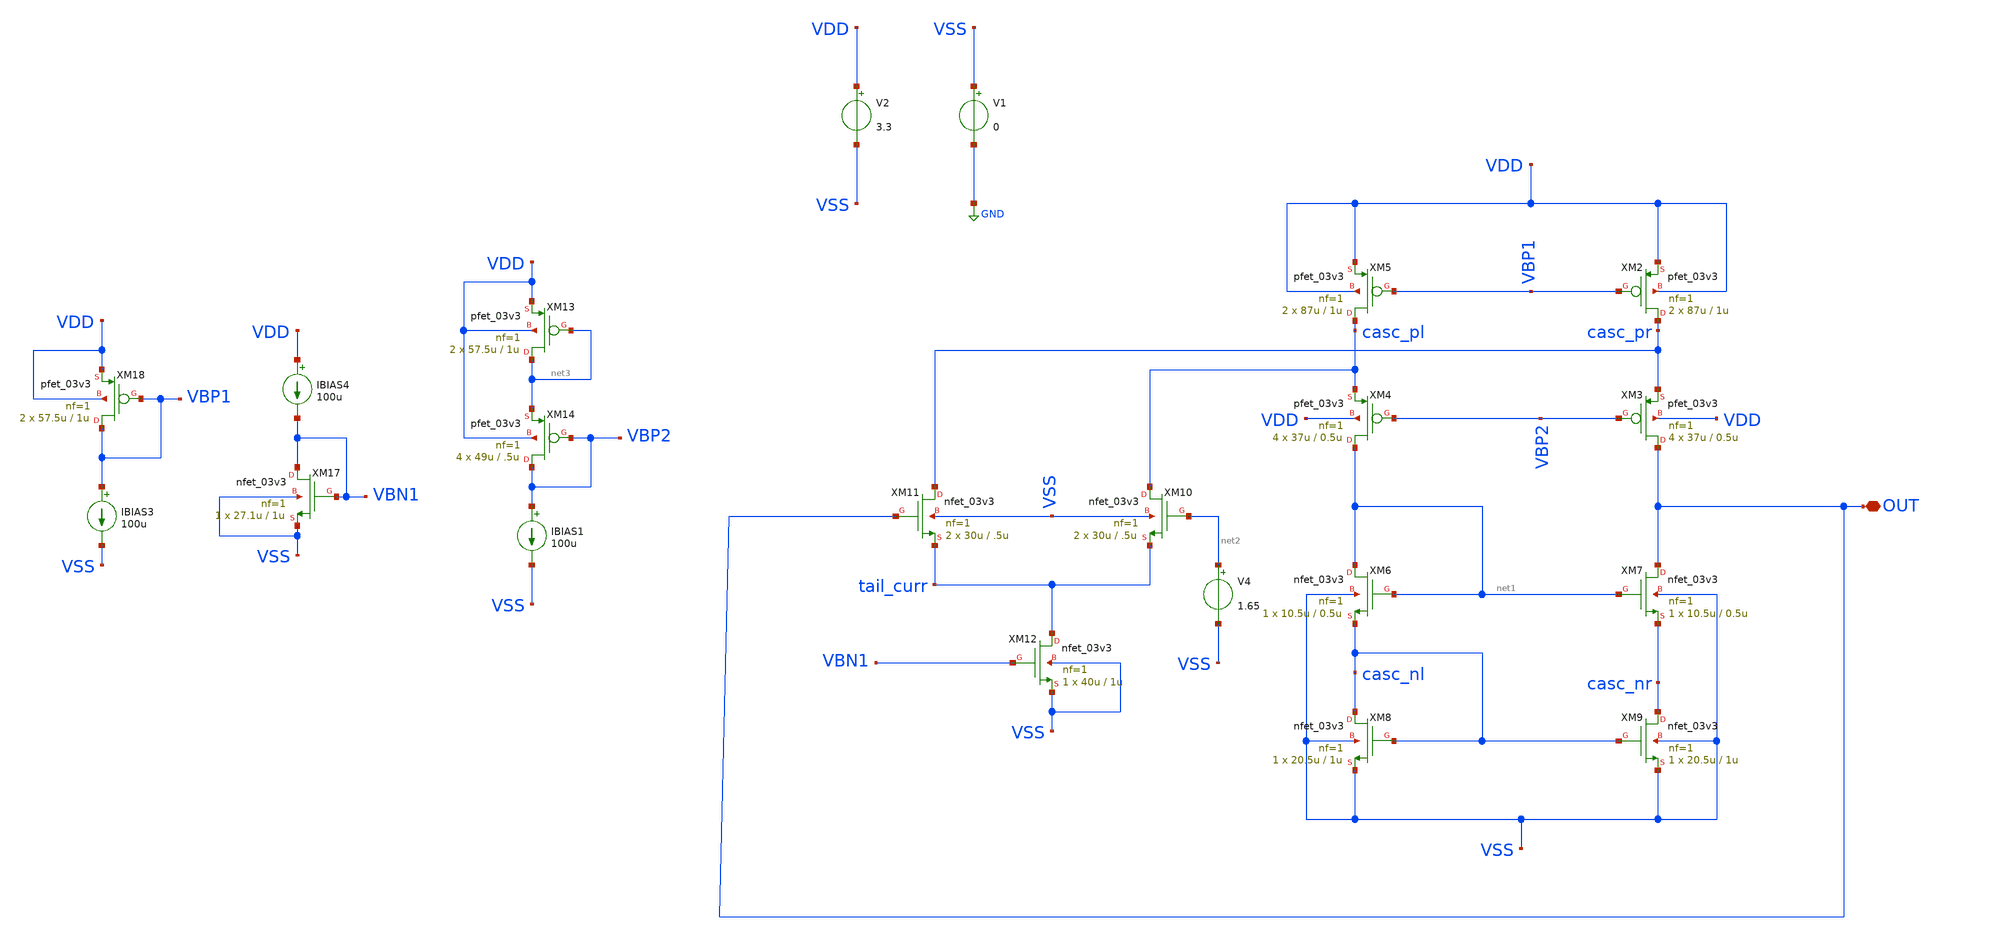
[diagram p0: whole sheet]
** sch_path: designs/untitled.sch
**.subckt untitled OUT
*.iopin OUT
XM2 casc_pr VBP1 VDD VDD pfet_03v3 L=1u W=87u nf=1 ad='int((nf+1)/2) * W/nf * 0.18u' as='int((nf+2)/2) * W/nf * 0.18u'
+ pd='2*int((nf+1)/2) * (W/nf + 0.18u)' ps='2*int((nf+2)/2) * (W/nf + 0.18u)' nrd='0.18u / W' nrs='0.18u / W'
+ sa=0 sb=0 sd=0 m=2
XM3 OUT VBP2 casc_pr VDD pfet_03v3 L=0.5u W=37u nf=1 ad='int((nf+1)/2) * W/nf * 0.18u' as='int((nf+2)/2) * W/nf * 0.18u'
+ pd='2*int((nf+1)/2) * (W/nf + 0.18u)' ps='2*int((nf+2)/2) * (W/nf + 0.18u)' nrd='0.18u / W' nrs='0.18u / W'
+ sa=0 sb=0 sd=0 m=4
XM4 net1 VBP2 casc_pl VDD pfet_03v3 L=0.5u W=37u nf=1 ad='int((nf+1)/2) * W/nf * 0.18u' as='int((nf+2)/2) * W/nf * 0.18u'
+ pd='2*int((nf+1)/2) * (W/nf + 0.18u)' ps='2*int((nf+2)/2) * (W/nf + 0.18u)' nrd='0.18u / W' nrs='0.18u / W'
+ sa=0 sb=0 sd=0 m=4
XM5 casc_pl VBP1 VDD VDD pfet_03v3 L=1u W=87u nf=1 ad='int((nf+1)/2) * W/nf * 0.18u' as='int((nf+2)/2) * W/nf * 0.18u'
+ pd='2*int((nf+1)/2) * (W/nf + 0.18u)' ps='2*int((nf+2)/2) * (W/nf + 0.18u)' nrd='0.18u / W' nrs='0.18u / W'
+ sa=0 sb=0 sd=0 m=2
XM6 net1 net1 casc_nl VSS nfet_03v3 L=0.5u W=10.5u nf=1 ad='int((nf+1)/2) * W/nf * 0.18u' as='int((nf+2)/2) * W/nf * 0.18u'
+ pd='2*int((nf+1)/2) * (W/nf + 0.18u)' ps='2*int((nf+2)/2) * (W/nf + 0.18u)' nrd='0.18u / W' nrs='0.18u / W'
+ sa=0 sb=0 sd=0 m=1
XM7 OUT net1 casc_nr VSS nfet_03v3 L=0.5u W=10.5u nf=1 ad='int((nf+1)/2) * W/nf * 0.18u' as='int((nf+2)/2) * W/nf * 0.18u'
+ pd='2*int((nf+1)/2) * (W/nf + 0.18u)' ps='2*int((nf+2)/2) * (W/nf + 0.18u)' nrd='0.18u / W' nrs='0.18u / W'
+ sa=0 sb=0 sd=0 m=1
XM8 casc_nl casc_nl VSS VSS nfet_03v3 L=1u W=20.5u nf=1 ad='int((nf+1)/2) * W/nf * 0.18u' as='int((nf+2)/2) * W/nf * 0.18u'
+ pd='2*int((nf+1)/2) * (W/nf + 0.18u)' ps='2*int((nf+2)/2) * (W/nf + 0.18u)' nrd='0.18u / W' nrs='0.18u / W'
+ sa=0 sb=0 sd=0 m=1
XM9 casc_nr casc_nl VSS VSS nfet_03v3 L=1u W=20.5u nf=1 ad='int((nf+1)/2) * W/nf * 0.18u' as='int((nf+2)/2) * W/nf * 0.18u'
+ pd='2*int((nf+1)/2) * (W/nf + 0.18u)' ps='2*int((nf+2)/2) * (W/nf + 0.18u)' nrd='0.18u / W' nrs='0.18u / W'
+ sa=0 sb=0 sd=0 m=1
XM10 casc_pl net2 tail_curr VSS nfet_03v3 L=.5u W=30u nf=1 ad='int((nf+1)/2) * W/nf * 0.18u' as='int((nf+2)/2) * W/nf * 0.18u'
+ pd='2*int((nf+1)/2) * (W/nf + 0.18u)' ps='2*int((nf+2)/2) * (W/nf + 0.18u)' nrd='0.18u / W' nrs='0.18u / W'
+ sa=0 sb=0 sd=0 m=2
XM12 tail_curr VBN1 VSS VSS nfet_03v3 L=1u W=40u nf=1 ad='int((nf+1)/2) * W/nf * 0.18u' as='int((nf+2)/2) * W/nf * 0.18u'
+ pd='2*int((nf+1)/2) * (W/nf + 0.18u)' ps='2*int((nf+2)/2) * (W/nf + 0.18u)' nrd='0.18u / W' nrs='0.18u / W'
+ sa=0 sb=0 sd=0 m=1
XM11 casc_pr OUT tail_curr VSS nfet_03v3 L=.5u W=30u nf=1 ad='int((nf+1)/2) * W/nf * 0.18u' as='int((nf+2)/2) * W/nf * 0.18u'
+ pd='2*int((nf+1)/2) * (W/nf + 0.18u)' ps='2*int((nf+2)/2) * (W/nf + 0.18u)' nrd='0.18u / W' nrs='0.18u / W'
+ sa=0 sb=0 sd=0 m=2
V2 VDD VSS 3.3
V1 VSS GND 0
V4 net2 VSS 1.65
XM13 net3 net3 VDD VDD pfet_03v3 L=1u W=57.5u nf=1 ad='int((nf+1)/2) * W/nf * 0.18u' as='int((nf+2)/2) * W/nf * 0.18u'
+ pd='2*int((nf+1)/2) * (W/nf + 0.18u)' ps='2*int((nf+2)/2) * (W/nf + 0.18u)' nrd='0.18u / W' nrs='0.18u / W'
+ sa=0 sb=0 sd=0 m=2
IBIAS1 VBP2 VSS 100u
XM14 VBP2 VBP2 net3 VDD pfet_03v3 L=.5u W=49u nf=1 ad='int((nf+1)/2) * W/nf * 0.18u' as='int((nf+2)/2) * W/nf * 0.18u'
+ pd='2*int((nf+1)/2) * (W/nf + 0.18u)' ps='2*int((nf+2)/2) * (W/nf + 0.18u)' nrd='0.18u / W' nrs='0.18u / W'
+ sa=0 sb=0 sd=0 m=4
XM17 VBN1 VBN1 VSS VSS nfet_03v3 L=1u W=27.1u nf=1 ad='int((nf+1)/2) * W/nf * 0.18u' as='int((nf+2)/2) * W/nf * 0.18u'
+ pd='2*int((nf+1)/2) * (W/nf + 0.18u)' ps='2*int((nf+2)/2) * (W/nf + 0.18u)' nrd='0.18u / W' nrs='0.18u / W'
+ sa=0 sb=0 sd=0 m=1
XM18 VBP1 VBP1 VDD VDD pfet_03v3 L=1u W=57.5u nf=1 ad='int((nf+1)/2) * W/nf * 0.18u' as='int((nf+2)/2) * W/nf * 0.18u'
+ pd='2*int((nf+1)/2) * (W/nf + 0.18u)' ps='2*int((nf+2)/2) * (W/nf + 0.18u)' nrd='0.18u / W' nrs='0.18u / W'
+ sa=0 sb=0 sd=0 m=2
IBIAS3 VBP1 VSS 100u
IBIAS4 VDD VBN1 100u
**.ends
.GLOBAL GND
.end
